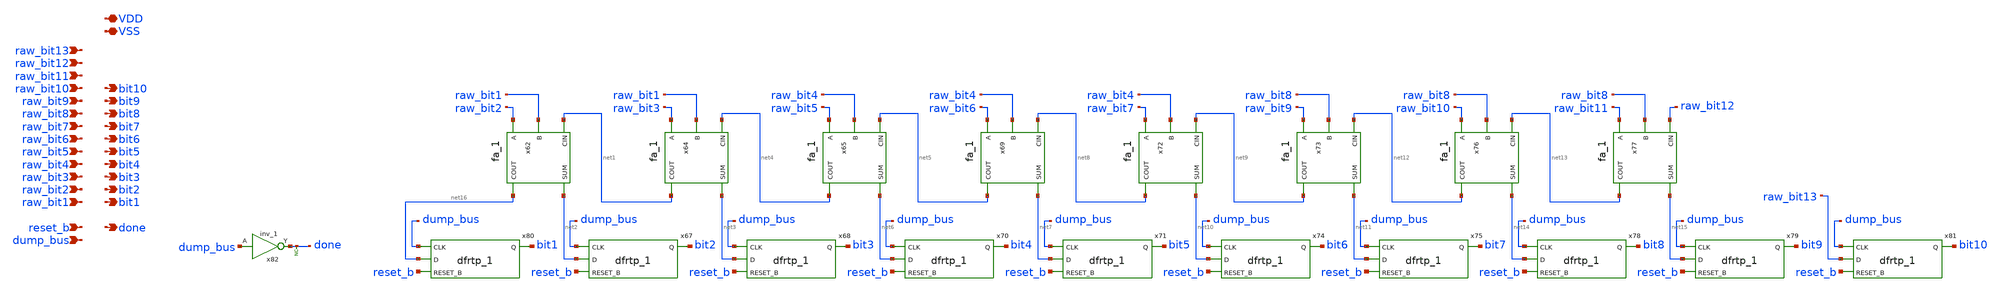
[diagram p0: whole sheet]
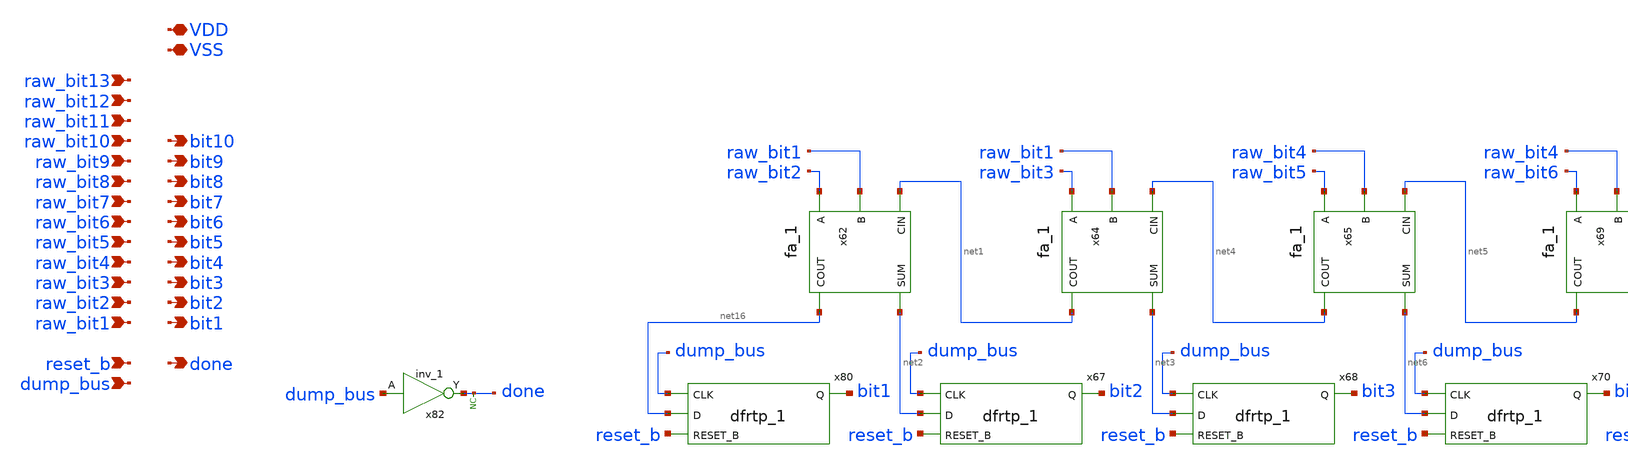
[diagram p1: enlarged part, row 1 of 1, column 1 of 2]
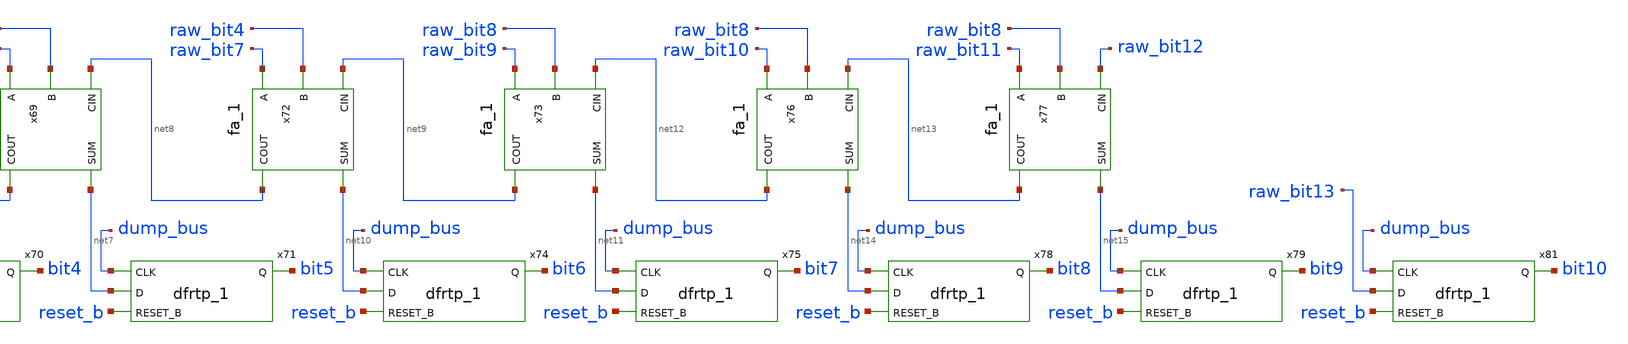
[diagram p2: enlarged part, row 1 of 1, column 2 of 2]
** sch_path: xschem/src/dec/dec.sch
**.subckt dec VDD VSS reset_b dump_bus done raw_bit13 raw_bit12 raw_bit11 raw_bit10 raw_bit9
*+ raw_bit8 raw_bit7 raw_bit6 raw_bit5 raw_bit4 raw_bit3 raw_bit2 raw_bit1 bit10 bit9 bit8 bit7 bit6 bit5 bit4
*+ bit3 bit2 bit1
*.iopin VDD
*.iopin VSS
*.ipin reset_b
*.ipin dump_bus
*.opin done
*.ipin raw_bit13
*.ipin raw_bit12
*.ipin raw_bit11
*.ipin raw_bit10
*.ipin raw_bit9
*.ipin raw_bit8
*.ipin raw_bit7
*.ipin raw_bit6
*.ipin raw_bit5
*.ipin raw_bit4
*.ipin raw_bit3
*.ipin raw_bit2
*.ipin raw_bit1
*.opin bit10
*.opin bit9
*.opin bit8
*.opin bit7
*.opin bit6
*.opin bit5
*.opin bit4
*.opin bit3
*.opin bit2
*.opin bit1
x62 raw_bit2 raw_bit1 net1 VSS VSS VDD VDD net16 net2 sky130_fd_sc_hd__fa_1
x64 raw_bit3 raw_bit1 net4 VSS VSS VDD VDD net1 net3 sky130_fd_sc_hd__fa_1
x67 dump_bus net2 reset_b VSS VSS VDD VDD bit2 sky130_fd_sc_hd__dfrtp_1
x68 dump_bus net3 reset_b VSS VSS VDD VDD bit3 sky130_fd_sc_hd__dfrtp_1
x65 raw_bit5 raw_bit4 net5 VSS VSS VDD VDD net4 net6 sky130_fd_sc_hd__fa_1
x69 raw_bit6 raw_bit4 net8 VSS VSS VDD VDD net5 net7 sky130_fd_sc_hd__fa_1
x70 dump_bus net6 reset_b VSS VSS VDD VDD bit4 sky130_fd_sc_hd__dfrtp_1
x71 dump_bus net7 reset_b VSS VSS VDD VDD bit5 sky130_fd_sc_hd__dfrtp_1
x72 raw_bit7 raw_bit4 net9 VSS VSS VDD VDD net8 net10 sky130_fd_sc_hd__fa_1
x73 raw_bit9 raw_bit8 net12 VSS VSS VDD VDD net9 net11 sky130_fd_sc_hd__fa_1
x74 dump_bus net10 reset_b VSS VSS VDD VDD bit6 sky130_fd_sc_hd__dfrtp_1
x75 dump_bus net11 reset_b VSS VSS VDD VDD bit7 sky130_fd_sc_hd__dfrtp_1
x76 raw_bit10 raw_bit8 net13 VSS VSS VDD VDD net12 net14 sky130_fd_sc_hd__fa_1
x77 raw_bit11 raw_bit8 raw_bit12 VSS VSS VDD VDD net13 net15 sky130_fd_sc_hd__fa_1
x78 dump_bus net14 reset_b VSS VSS VDD VDD bit8 sky130_fd_sc_hd__dfrtp_1
x79 dump_bus net15 reset_b VSS VSS VDD VDD bit9 sky130_fd_sc_hd__dfrtp_1
x80 dump_bus net16 reset_b VSS VSS VDD VDD bit1 sky130_fd_sc_hd__dfrtp_1
x81 dump_bus raw_bit13 reset_b VSS VSS VDD VDD bit10 sky130_fd_sc_hd__dfrtp_1
x82 dump_bus VSS VSS VDD VDD done sky130_fd_sc_hd__inv_1
* noconn done
**.ends
.end
